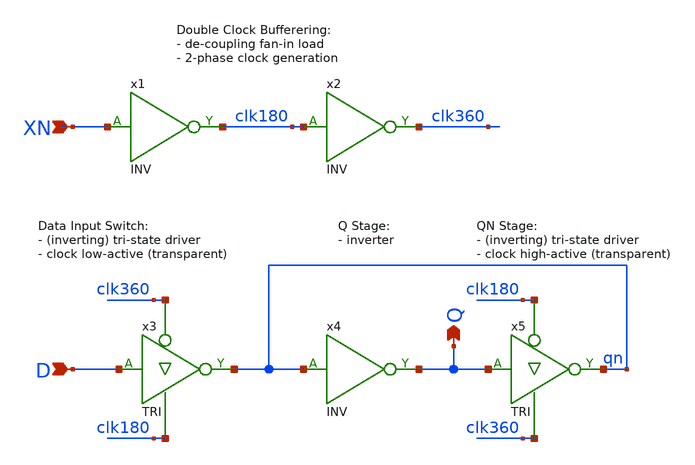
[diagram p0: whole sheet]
** sch_path: Sources/crafted/LATN.sch
**.subckt LATN XN D Q
*.ipin XN
*.ipin D
*.opin Q
x1 XN clk180 VDD GND INV Wmin=1.5u Lmin=1u g=2 m=1
x2 clk180 clk360 VDD GND INV Wmin=1.5u Lmin=1u g=2 m=1
x4 qn Q VDD GND INV Wmin=1.5u Lmin=1u g=2 m=1
x3 D clk360 clk180 qn VDD GND TRI Wmin=1.5u Lmin=1u g=2 m=1
x5 Q clk180 clk360 qn VDD GND TRI Wmin=1.5u Lmin=1u g=2 m=1
**.ends
.end
